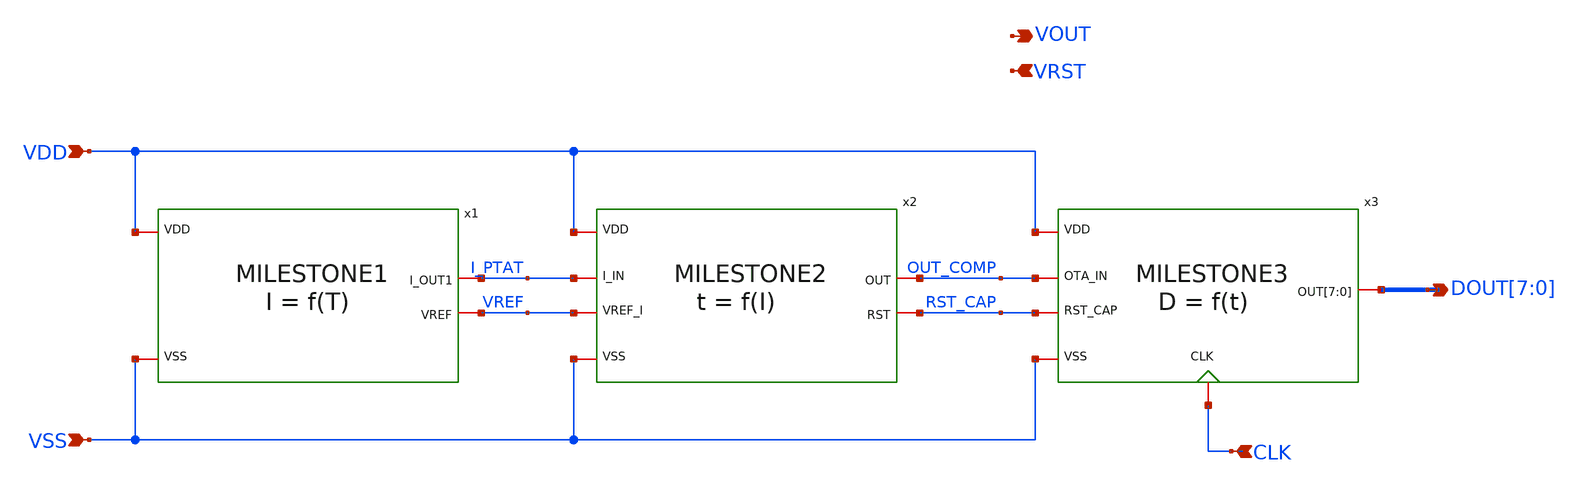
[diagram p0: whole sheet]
** sch_path: design/CNR_GR03_SKY130NM/TOPLEVEL.sch
**.subckt TOPLEVEL VDD VSS VOUT VRST CLK
*+ DOUT[7],DOUT[6],DOUT[5],DOUT[4],DOUT[3],DOUT[2],DOUT[1],DOUT[0]
*.ipin VDD
*.ipin VSS
*.opin VOUT
*.ipin VRST
*.ipin CLK
*.opin DOUT[7],DOUT[6],DOUT[5],DOUT[4],DOUT[3],DOUT[2],DOUT[1],DOUT[0]
x1 VDD I_PTAT VREF VSS MILESTONE1
x2 I_PTAT VREF OUT_COMP VDD RST_CAP VSS MILESTONE2
x3 OUT_COMP RST_CAP CLK DOUT[7] DOUT[6] DOUT[5] DOUT[4] DOUT[3] DOUT[2] DOUT[1] DOUT[0] VDD VSS
+ MILESTONE3
**.ends
.end
